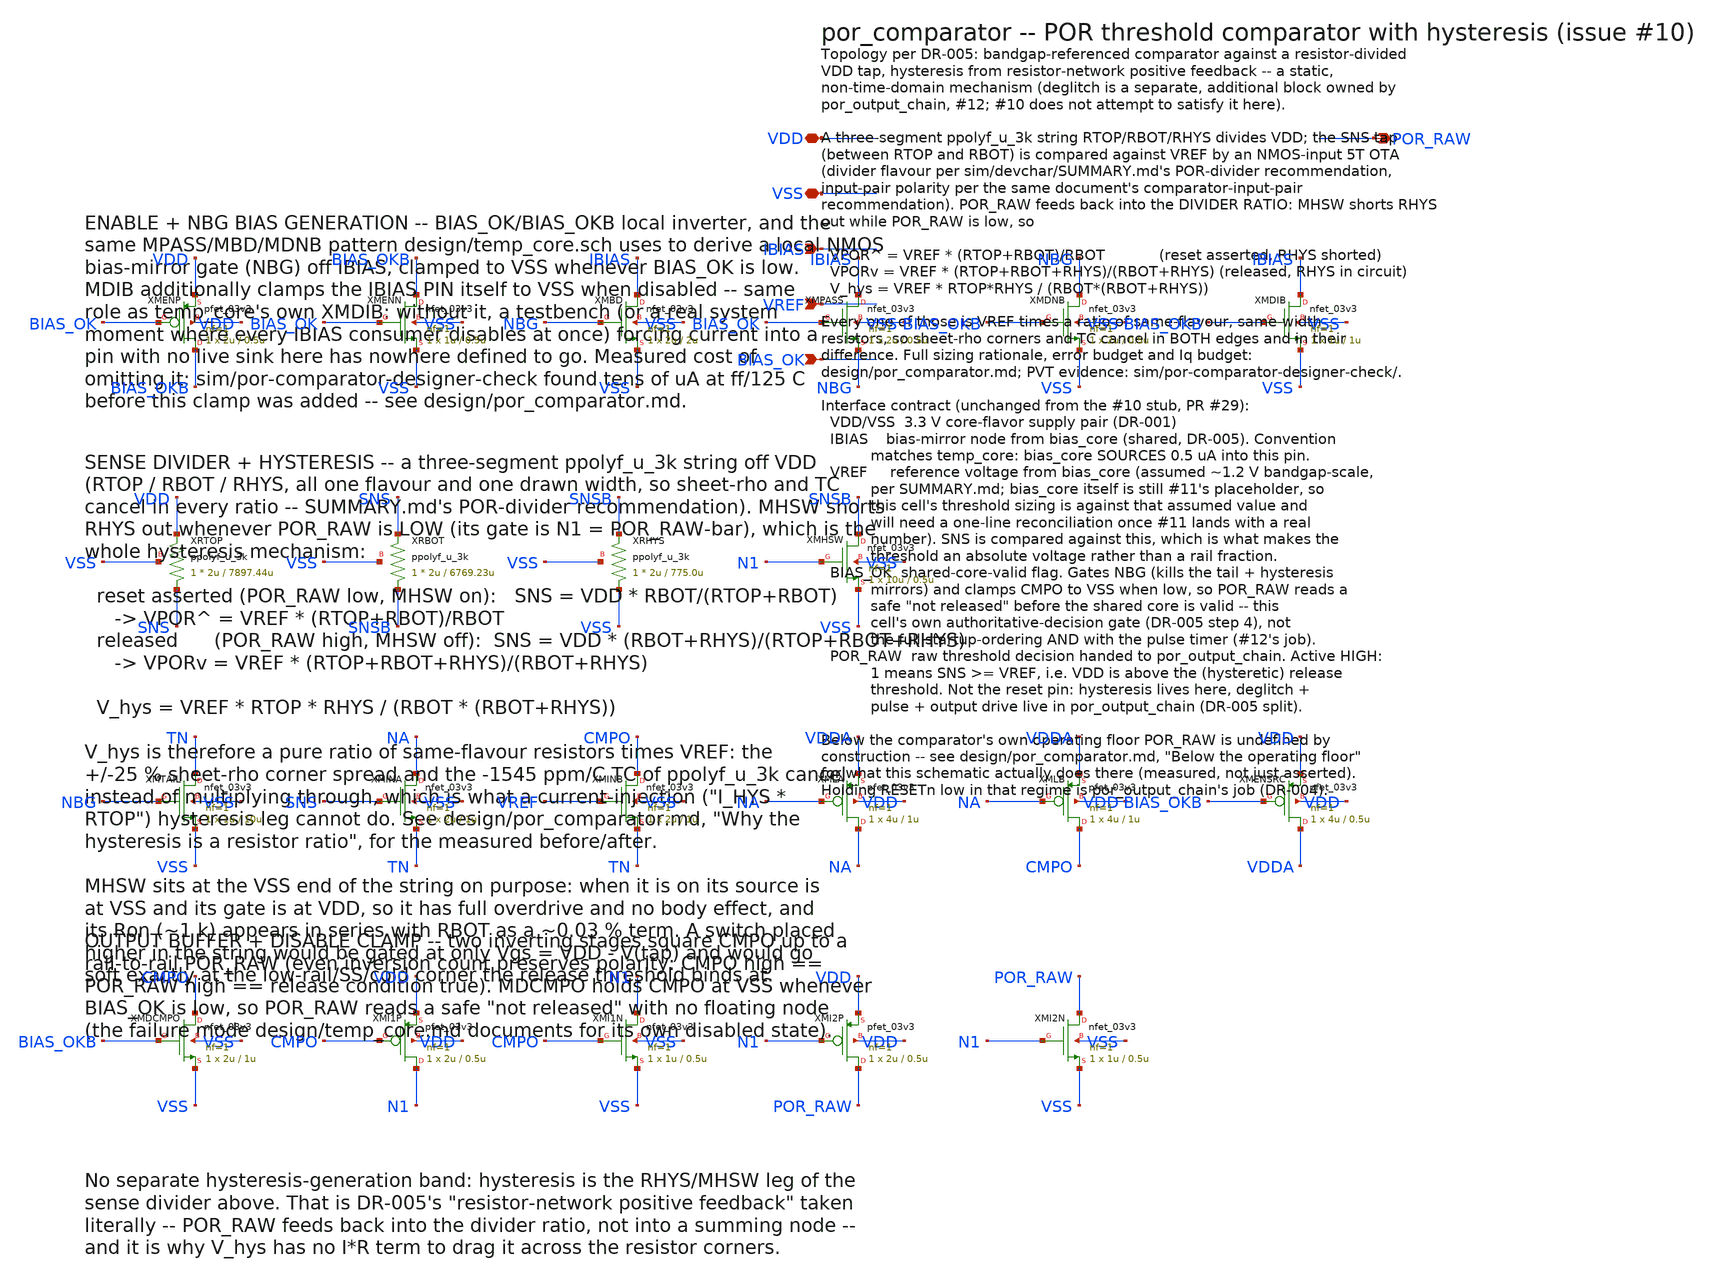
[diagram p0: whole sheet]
** sch_path: design/por_comparator.sch
**.subckt por_comparator VDD VSS IBIAS VREF BIAS_OK POR_RAW
*.iopin VDD
*.iopin VSS
*.ipin IBIAS
*.ipin VREF
*.ipin BIAS_OK
*.opin POR_RAW
XMENP BIAS_OKB BIAS_OK VDD VDD pfet_03v3 L=0.5u W=2u nf=1 ad='int((nf+1)/2) * W/nf * 0.18u' as='int((nf+2)/2) * W/nf * 0.18u'
+ pd='2*int((nf+1)/2) * (W/nf + 0.18u)' ps='2*int((nf+2)/2) * (W/nf + 0.18u)' nrd='0.18u / W' nrs='0.18u / W'
+ sa=0 sb=0 sd=0 m=1
XMENN BIAS_OKB BIAS_OK VSS VSS nfet_03v3 L=0.5u W=1u nf=1 ad='int((nf+1)/2) * W/nf * 0.18u' as='int((nf+2)/2) * W/nf * 0.18u'
+ pd='2*int((nf+1)/2) * (W/nf + 0.18u)' ps='2*int((nf+2)/2) * (W/nf + 0.18u)' nrd='0.18u / W' nrs='0.18u / W'
+ sa=0 sb=0 sd=0 m=1
XMBD IBIAS NBG VSS VSS nfet_03v3 L=2u W=2u nf=1 ad='int((nf+1)/2) * W/nf * 0.18u' as='int((nf+2)/2) * W/nf * 0.18u'
+ pd='2*int((nf+1)/2) * (W/nf + 0.18u)' ps='2*int((nf+2)/2) * (W/nf + 0.18u)' nrd='0.18u / W' nrs='0.18u / W'
+ sa=0 sb=0 sd=0 m=1
XMPASS IBIAS BIAS_OK NBG VSS nfet_03v3 L=0.5u W=2u nf=1 ad='int((nf+1)/2) * W/nf * 0.18u' as='int((nf+2)/2) * W/nf * 0.18u'
+ pd='2*int((nf+1)/2) * (W/nf + 0.18u)' ps='2*int((nf+2)/2) * (W/nf + 0.18u)' nrd='0.18u / W' nrs='0.18u / W'
+ sa=0 sb=0 sd=0 m=1
XMDNB NBG BIAS_OKB VSS VSS nfet_03v3 L=0.5u W=2u nf=1 ad='int((nf+1)/2) * W/nf * 0.18u' as='int((nf+2)/2) * W/nf * 0.18u'
+ pd='2*int((nf+1)/2) * (W/nf + 0.18u)' ps='2*int((nf+2)/2) * (W/nf + 0.18u)' nrd='0.18u / W' nrs='0.18u / W'
+ sa=0 sb=0 sd=0 m=1
XMDIB IBIAS BIAS_OKB VSS VSS nfet_03v3 L=1u W=1u nf=1 ad='int((nf+1)/2) * W/nf * 0.18u' as='int((nf+2)/2) * W/nf * 0.18u'
+ pd='2*int((nf+1)/2) * (W/nf + 0.18u)' ps='2*int((nf+2)/2) * (W/nf + 0.18u)' nrd='0.18u / W' nrs='0.18u / W'
+ sa=0 sb=0 sd=0 m=1
XRTOP SNS VDD VSS ppolyf_u_3k r_width=2u r_length=7897.44u m=1
XRBOT SNSB SNS VSS ppolyf_u_3k r_width=2u r_length=6769.23u m=1
XRHYS VSS SNSB VSS ppolyf_u_3k r_width=2u r_length=775.0u m=1
XMHSW SNSB N1 VSS VSS nfet_03v3 L=0.5u W=10u nf=1 ad='int((nf+1)/2) * W/nf * 0.18u' as='int((nf+2)/2) * W/nf * 0.18u'
+ pd='2*int((nf+1)/2) * (W/nf + 0.18u)' ps='2*int((nf+2)/2) * (W/nf + 0.18u)' nrd='0.18u / W' nrs='0.18u / W'
+ sa=0 sb=0 sd=0 m=1
XMTAIL TN NBG VSS VSS nfet_03v3 L=10u W=1u nf=1 ad='int((nf+1)/2) * W/nf * 0.18u' as='int((nf+2)/2) * W/nf * 0.18u'
+ pd='2*int((nf+1)/2) * (W/nf + 0.18u)' ps='2*int((nf+2)/2) * (W/nf + 0.18u)' nrd='0.18u / W' nrs='0.18u / W'
+ sa=0 sb=0 sd=0 m=1
XMINA NA SNS TN VSS nfet_03v3 L=1u W=2u nf=1 ad='int((nf+1)/2) * W/nf * 0.18u' as='int((nf+2)/2) * W/nf * 0.18u'
+ pd='2*int((nf+1)/2) * (W/nf + 0.18u)' ps='2*int((nf+2)/2) * (W/nf + 0.18u)' nrd='0.18u / W' nrs='0.18u / W'
+ sa=0 sb=0 sd=0 m=1
XMINB CMPO VREF TN VSS nfet_03v3 L=1u W=2u nf=1 ad='int((nf+1)/2) * W/nf * 0.18u' as='int((nf+2)/2) * W/nf * 0.18u'
+ pd='2*int((nf+1)/2) * (W/nf + 0.18u)' ps='2*int((nf+2)/2) * (W/nf + 0.18u)' nrd='0.18u / W' nrs='0.18u / W'
+ sa=0 sb=0 sd=0 m=1
XMLA NA NA VDDA VDD pfet_03v3 L=1u W=4u nf=1 ad='int((nf+1)/2) * W/nf * 0.18u' as='int((nf+2)/2) * W/nf * 0.18u'
+ pd='2*int((nf+1)/2) * (W/nf + 0.18u)' ps='2*int((nf+2)/2) * (W/nf + 0.18u)' nrd='0.18u / W' nrs='0.18u / W'
+ sa=0 sb=0 sd=0 m=1
XMLB CMPO NA VDDA VDD pfet_03v3 L=1u W=4u nf=1 ad='int((nf+1)/2) * W/nf * 0.18u' as='int((nf+2)/2) * W/nf * 0.18u'
+ pd='2*int((nf+1)/2) * (W/nf + 0.18u)' ps='2*int((nf+2)/2) * (W/nf + 0.18u)' nrd='0.18u / W' nrs='0.18u / W'
+ sa=0 sb=0 sd=0 m=1
XMENSRC VDDA BIAS_OKB VDD VDD pfet_03v3 L=0.5u W=4u nf=1 ad='int((nf+1)/2) * W/nf * 0.18u' as='int((nf+2)/2) * W/nf * 0.18u'
+ pd='2*int((nf+1)/2) * (W/nf + 0.18u)' ps='2*int((nf+2)/2) * (W/nf + 0.18u)' nrd='0.18u / W' nrs='0.18u / W'
+ sa=0 sb=0 sd=0 m=1
XMDCMPO CMPO BIAS_OKB VSS VSS nfet_03v3 L=1u W=2u nf=1 ad='int((nf+1)/2) * W/nf * 0.18u' as='int((nf+2)/2) * W/nf * 0.18u'
+ pd='2*int((nf+1)/2) * (W/nf + 0.18u)' ps='2*int((nf+2)/2) * (W/nf + 0.18u)' nrd='0.18u / W' nrs='0.18u / W'
+ sa=0 sb=0 sd=0 m=1
XMI1P N1 CMPO VDD VDD pfet_03v3 L=0.5u W=2u nf=1 ad='int((nf+1)/2) * W/nf * 0.18u' as='int((nf+2)/2) * W/nf * 0.18u'
+ pd='2*int((nf+1)/2) * (W/nf + 0.18u)' ps='2*int((nf+2)/2) * (W/nf + 0.18u)' nrd='0.18u / W' nrs='0.18u / W'
+ sa=0 sb=0 sd=0 m=1
XMI1N N1 CMPO VSS VSS nfet_03v3 L=0.5u W=1u nf=1 ad='int((nf+1)/2) * W/nf * 0.18u' as='int((nf+2)/2) * W/nf * 0.18u'
+ pd='2*int((nf+1)/2) * (W/nf + 0.18u)' ps='2*int((nf+2)/2) * (W/nf + 0.18u)' nrd='0.18u / W' nrs='0.18u / W'
+ sa=0 sb=0 sd=0 m=1
XMI2P POR_RAW N1 VDD VDD pfet_03v3 L=0.5u W=2u nf=1 ad='int((nf+1)/2) * W/nf * 0.18u' as='int((nf+2)/2) * W/nf * 0.18u'
+ pd='2*int((nf+1)/2) * (W/nf + 0.18u)' ps='2*int((nf+2)/2) * (W/nf + 0.18u)' nrd='0.18u / W' nrs='0.18u / W'
+ sa=0 sb=0 sd=0 m=1
XMI2N POR_RAW N1 VSS VSS nfet_03v3 L=0.5u W=1u nf=1 ad='int((nf+1)/2) * W/nf * 0.18u' as='int((nf+2)/2) * W/nf * 0.18u'
+ pd='2*int((nf+1)/2) * (W/nf + 0.18u)' ps='2*int((nf+2)/2) * (W/nf + 0.18u)' nrd='0.18u / W' nrs='0.18u / W'
+ sa=0 sb=0 sd=0 m=1
**.ends
.end
